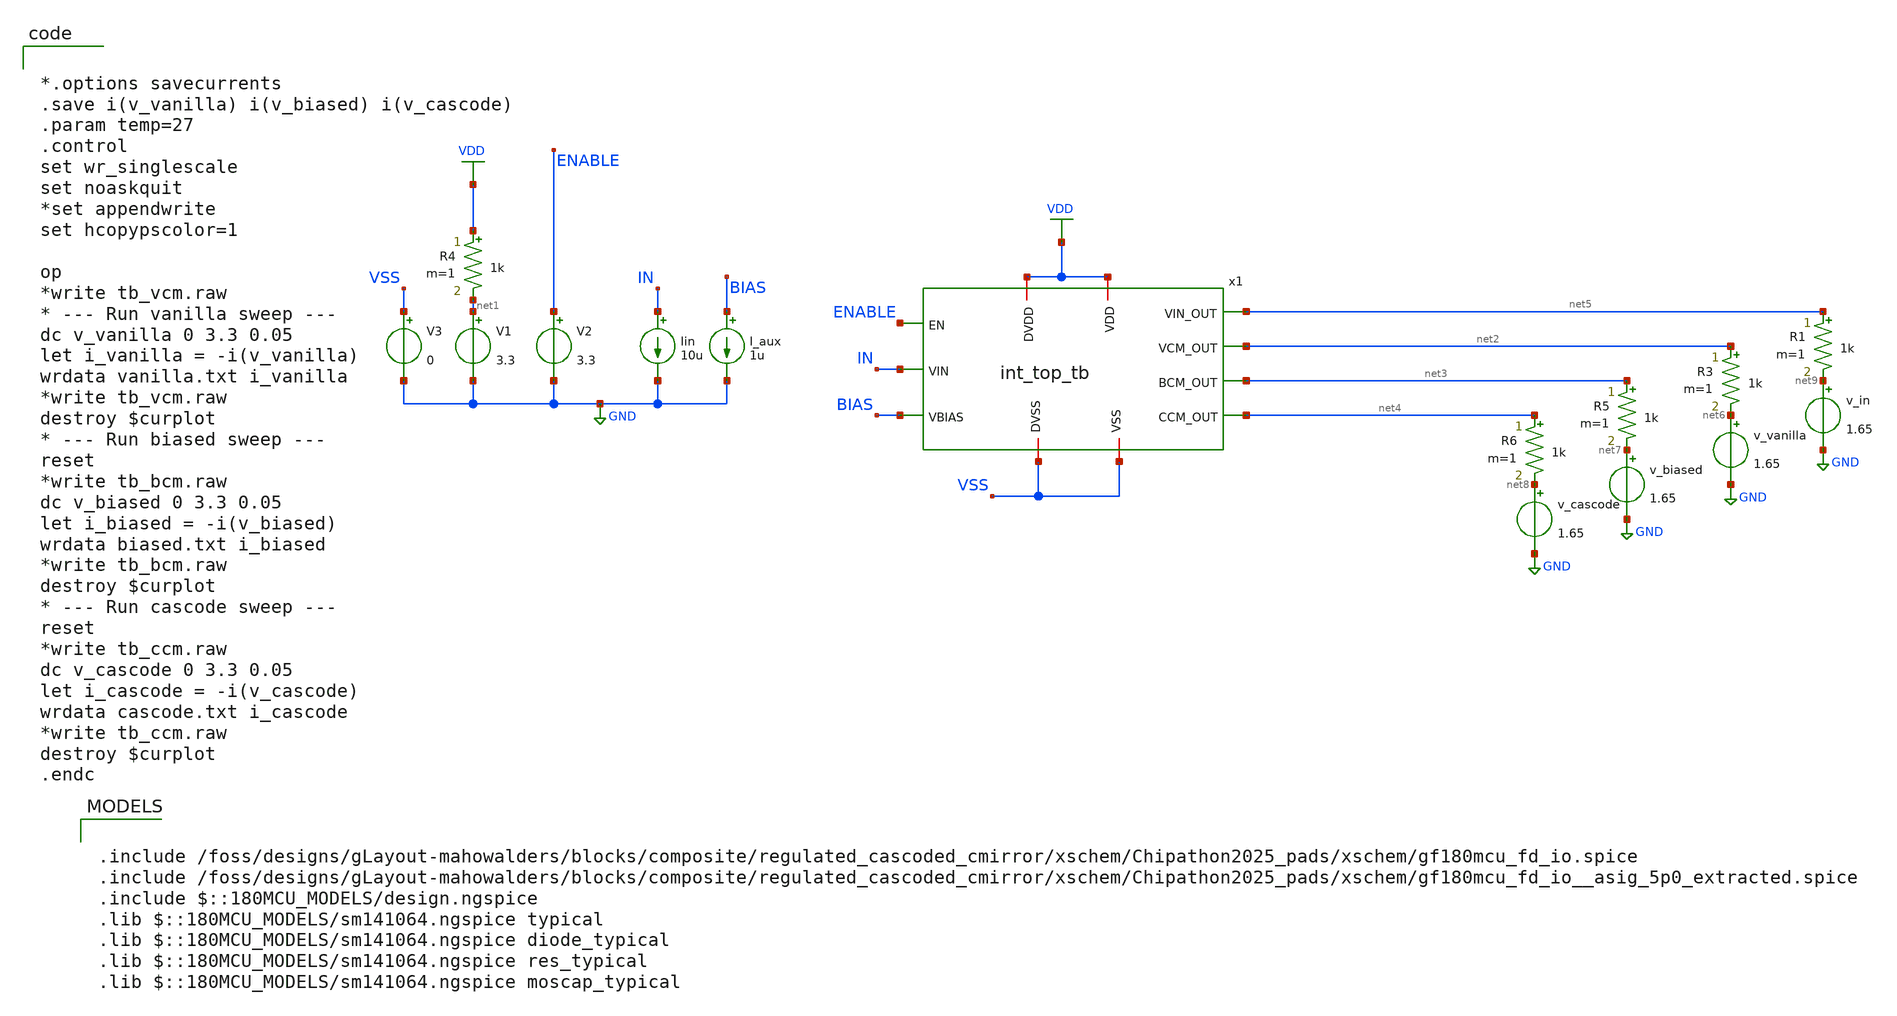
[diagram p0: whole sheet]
** sch_path: blocks/composite/regulated_cascoded_cmirror/xschem/chip_top.sch
**.subckt chip_top
v_vanilla net6 GND 1.65
v_biased net7 GND 1.65
v_cascode net8 GND 1.65
R3 net2 net6 1k m=1
R5 net3 net7 1k m=1
R6 net4 net8 1k m=1
V1 net1 GND 3.3
R4 VDD net1 1k m=1
x1 net2 ENABLE net3 net4 IN VSS VDD VDD VSS BIAS net5 int_top_tb
V2 ENABLE GND 3.3
Iin IN GND 10u
I_aux BIAS GND 1u
V3 VSS GND 0
v_in net9 GND 1.65
R1 net5 net9 1k m=1
**** begin user architecture code

.include /foss/designs/gLayout-mahowalders/blocks/composite/regulated_cascoded_cmirror/xschem/Chipathon2025_pads/xschem/gf180mcu_fd_io.spice
.include /foss/designs/gLayout-mahowalders/blocks/composite/regulated_cascoded_cmirror/xschem/Chipathon2025_pads/xschem/gf180mcu_fd_io__asig_5p0_extracted.spice
.include $::180MCU_MODELS/design.ngspice
.lib $::180MCU_MODELS/sm141064.ngspice typical
.lib $::180MCU_MODELS/sm141064.ngspice diode_typical
.lib $::180MCU_MODELS/sm141064.ngspice res_typical
.lib $::180MCU_MODELS/sm141064.ngspice moscap_typical



*.options savecurrents
.save i(v_vanilla) i(v_biased) i(v_cascode)
.param temp=27
.control
set wr_singlescale
set noaskquit
*set appendwrite
set hcopypscolor=1

op
*write tb_vcm.raw
* --- Run vanilla sweep ---
dc v_vanilla 0 3.3 0.05
let i_vanilla = -i(v_vanilla)
wrdata vanilla.txt i_vanilla
*write tb_vcm.raw
destroy $curplot
* --- Run biased sweep ---
reset
*write tb_bcm.raw
dc v_biased 0 3.3 0.05
let i_biased = -i(v_biased)
wrdata biased.txt i_biased
*write tb_bcm.raw
destroy $curplot
* --- Run cascode sweep ---
reset
*write tb_ccm.raw
dc v_cascode 0 3.3 0.05
let i_cascode = -i(v_cascode)
wrdata cascode.txt i_cascode
*write tb_ccm.raw
destroy $curplot
.endc


**** end user architecture code
**.ends
.GLOBAL GND
.GLOBAL VDD
.end
